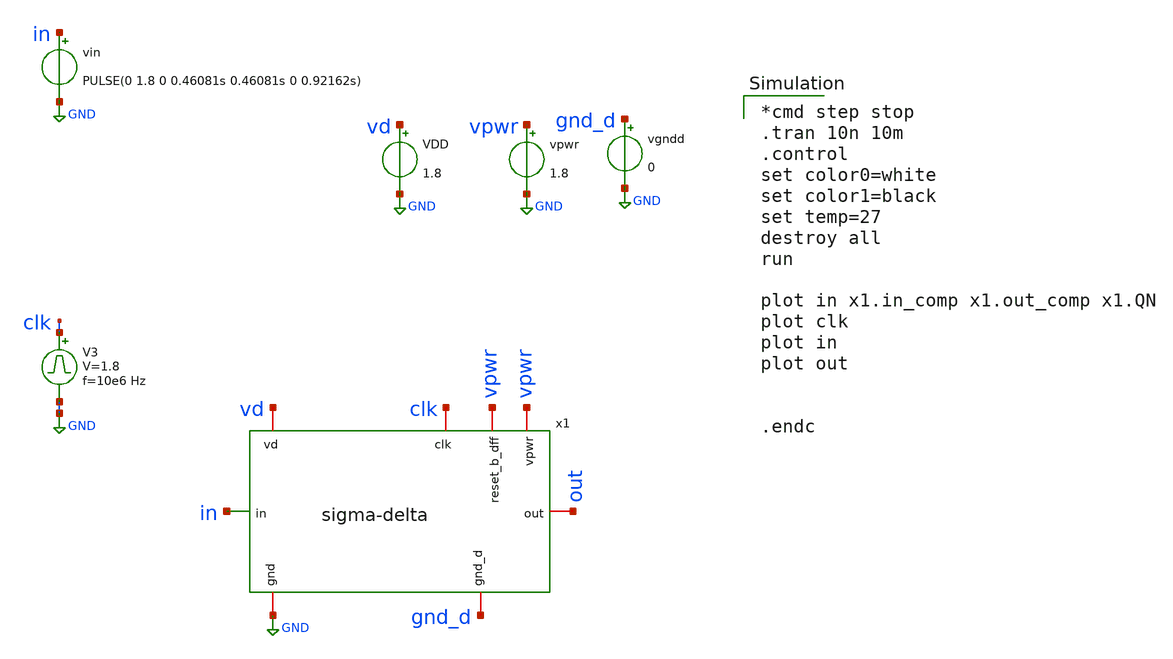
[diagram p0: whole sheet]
** sch_path: sigma-delta_modulator/xschem/sigma_tb-tran.sch
* Copyright 2020 Stefan Frederik Schippers
* Licensed under the Apache License, Version 2.0 (the "License");
* you may not use this file except in compliance with the License.
* You may obtain a copy of the License at
* https://www.apache.org/licenses/LICENSE-2.0
* Unless required by applicable law or agreed to in writing, software
* distributed under the License is distributed on an "AS IS" BASIS,
* WITHOUT WARRANTIES OR CONDITIONS OF ANY KIND, either express or implied.
* See the License for the specific language governing permissions and
* limitations under the License.
**.subckt sigma_tb-tran
VDD vd GND 1.8
vin in GND PULSE(0 1.8 0 0.46081s 0.46081s 0 0.92162s)
vpwr vpwr GND 1.8
vgndd gnd_d GND 0
V3 clk GND pulse 0 1.8 '0.495/ 10e6 ' '0.01/10e6 ' '0.01/10e6 ' '0.49/10e6 ' '1/10e6 '
x1 gnd_d vpwr clk vd out in vpwr GND sigma-delta
**** begin user architecture code

*cmd step stop
.tran 10n 10m
.control
set color0=white
set color1=black
set temp=27
destroy all
run

plot in x1.in_comp x1.out_comp x1.QN
plot clk
plot in
plot out


.endc

 .lib $::SKYWATER_MODELS/sky130.lib.spice tt
.include $::SKYWATER_STDCELLS/sky130_fd_sc_hd.spice

**** end user architecture code
**.ends

* expanding   symbol:
*+  /home/hugodg/projects-sky130/temp-sensor/sigma-delta_modulator/xschem/sigma-delta.sym # of pins=8
** sym_path: sigma-delta_modulator/xschem/sigma-delta.sym
** sch_path: sigma-delta_modulator/xschem/sigma-delta.sch
.subckt sigma-delta gnd_d vpwr clk vd out in reset_b_dff gnd
*.ipin in
*.iopin gnd
*.iopin clk
*.iopin out
*.iopin reset_b_dff
*.iopin vpwr
*.iopin gnd_d
*.iopin vd
**** begin user architecture code




**** end user architecture code
XC1 in_comp gnd sky130_fd_pr__cap_mim_m3_1 W=27.196 L=27.196 MF=1 m=1
XR2 QN in_comp gnd sky130_fd_pr__res_xhigh_po_0p35 L=36 mult=1 m=1
XR1 in_comp in gnd sky130_fd_pr__res_xhigh_po_0p35 L=36 mult=1 m=1
XN1 out_comp in_comp gnd gnd sky130_fd_pr__nfet_01v8 L=0.15 W=1 nf=1 ad='int((nf+1)/2) * W/nf * 0.29'
+ as='int((nf+2)/2) * W/nf * 0.29' pd='2*int((nf+1)/2) * (W/nf + 0.29)' ps='2*int((nf+2)/2) * (W/nf + 0.29)'
+ nrd='0.29 / W' nrs='0.29 / W' sa=0 sb=0 sd=0 mult=1 m=1
XP1 out_comp in_comp vd vd sky130_fd_pr__pfet_01v8 L=0.15 W=3 nf=1 ad='int((nf+1)/2) * W/nf * 0.29' as='int((nf+2)/2) * W/nf * 0.29'
+ pd='2*int((nf+1)/2) * (W/nf + 0.29)' ps='2*int((nf+2)/2) * (W/nf + 0.29)' nrd='0.29 / W' nrs='0.29 / W'
+ sa=0 sb=0 sd=0 mult=1 m=1
x1 clk out_comp reset_b_dff GND_D GND_D VPWR VPWR QN out sky130_fd_sc_hd__dfrbp_1
.ends

.GLOBAL GND
.end
